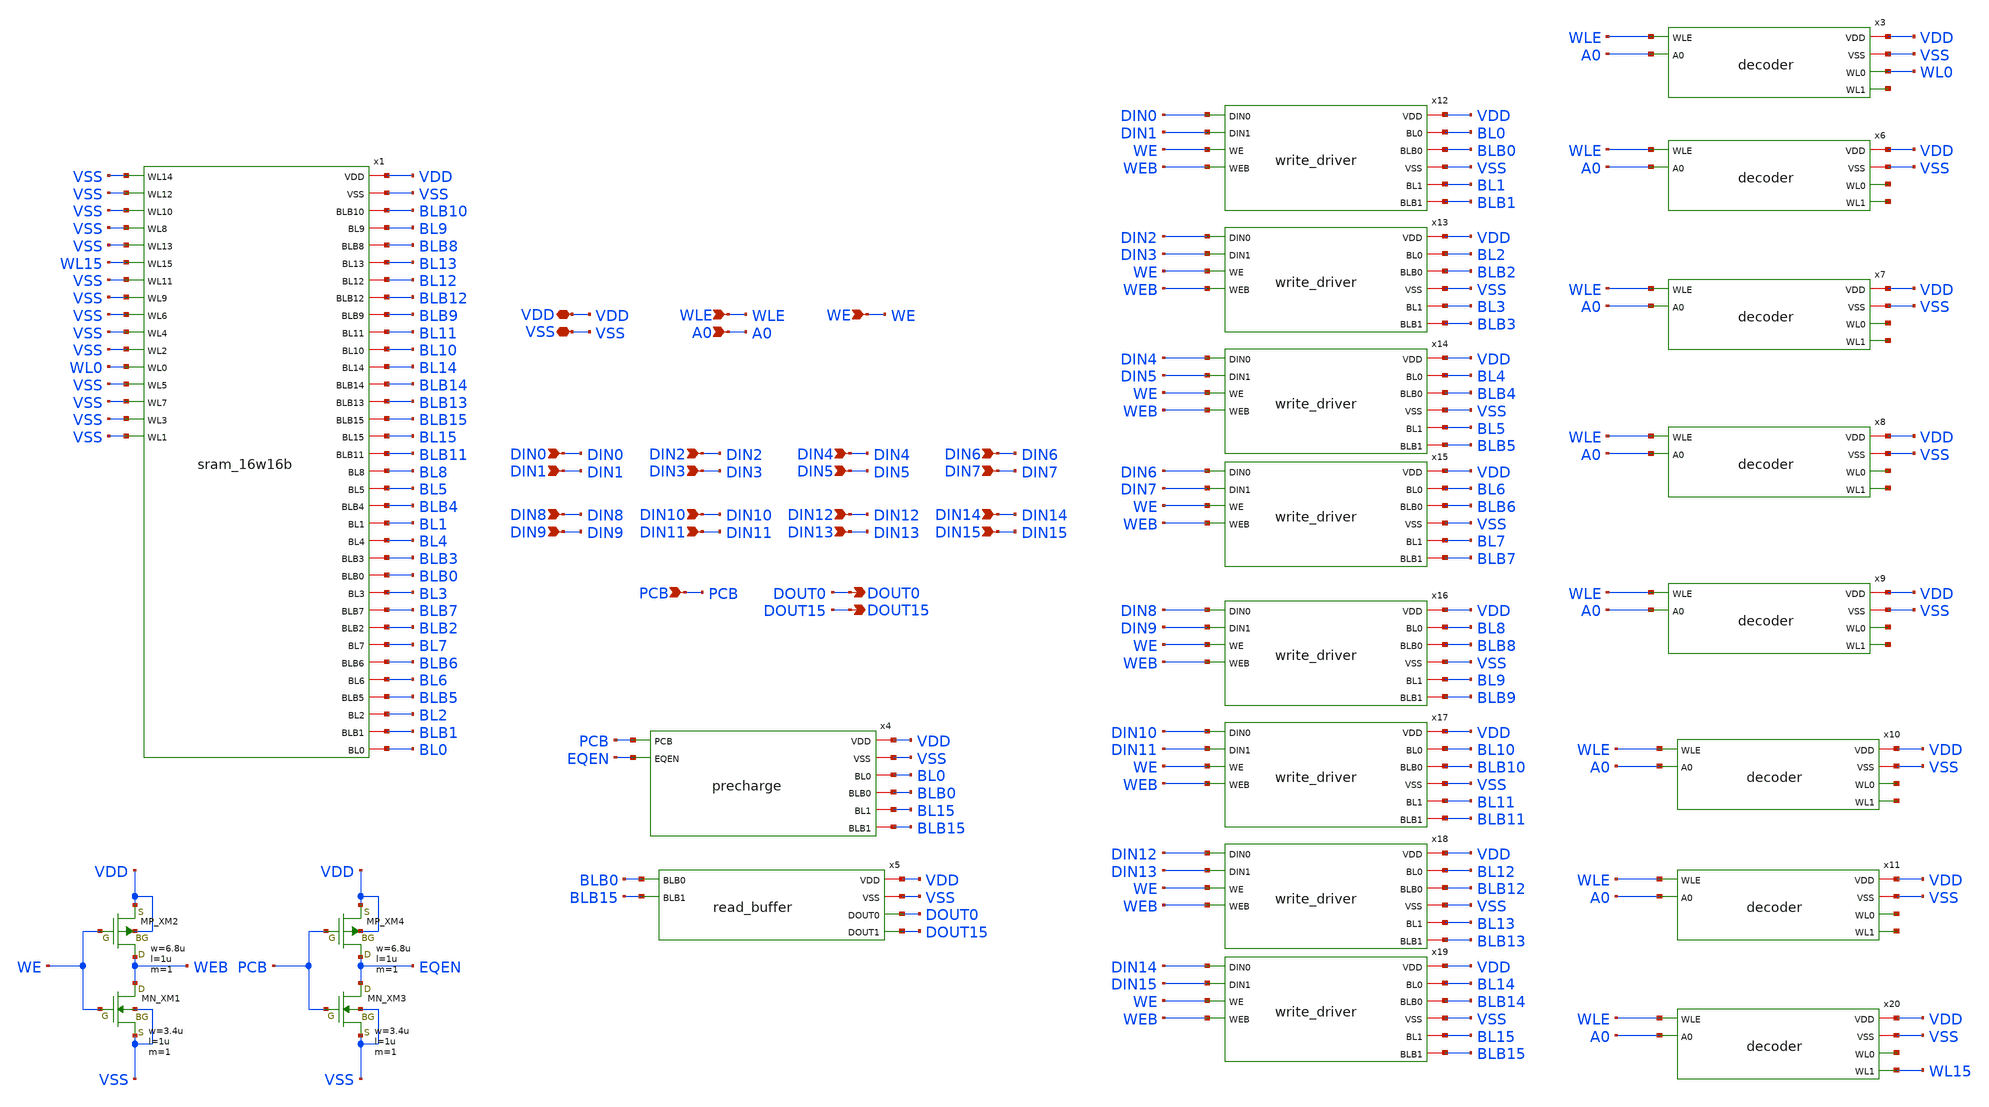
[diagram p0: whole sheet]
** sch_path: sram/sram_16w16b_top.sch
**.subckt sram_16w16b_top VDD WLE DOUT0 VSS A0 WE DIN0 DIN1 PCB DOUT15 DIN2 DIN3 DIN4 DIN5 DIN6 DIN7
*+ DIN8 DIN9 DIN10 DIN11 DIN12 DIN13 DIN14 DIN15
*.iopin VDD
*.ipin WLE
*.opin DOUT0
*.iopin VSS
*.ipin A0
*.ipin WE
*.ipin DIN0
*.ipin DIN1
*.ipin PCB
*.opin DOUT15
*.ipin DIN2
*.ipin DIN3
*.ipin DIN4
*.ipin DIN5
*.ipin DIN6
*.ipin DIN7
*.ipin DIN8
*.ipin DIN9
*.ipin DIN10
*.ipin DIN11
*.ipin DIN12
*.ipin DIN13
*.ipin DIN14
*.ipin DIN15
x4 VDD VSS PCB EQEN BL0 BLB0 BL15 BLB15 precharge
x5 VDD VSS BLB0 BLB15 DOUT0 DOUT15 read_buffer
XXM1 WEB WE VSS VSS NMOS w=3.4u l=1u nrd=0 nrs=0 m=1
XXM2 WEB WE VDD VDD PMOS w=6.8u l=1u nrd=0 nrs=0 m=1
XXM3 EQEN PCB VSS VSS NMOS w=3.4u l=1u nrd=0 nrs=0 m=1
XXM4 EQEN PCB VDD VDD PMOS w=6.8u l=1u nrd=0 nrs=0 m=1
x12 DIN0 VDD BL0 BLB0 VSS DIN1 BL1 WE BLB1 WEB write_driver
x13 DIN2 VDD BL2 BLB2 VSS DIN3 BL3 WE BLB3 WEB write_driver
x14 DIN4 VDD BL4 BLB4 VSS DIN5 BL5 WE BLB5 WEB write_driver
x15 DIN6 VDD BL6 BLB6 VSS DIN7 BL7 WE BLB7 WEB write_driver
x16 DIN8 VDD BL8 BLB8 VSS DIN9 BL9 WE BLB9 WEB write_driver
x17 DIN10 VDD BL10 BLB10 VSS DIN11 BL11 WE BLB11 WEB write_driver
x18 DIN12 VDD BL12 BLB12 VSS DIN13 BL13 WE BLB13 WEB write_driver
x19 DIN14 VDD BL14 BLB14 VSS DIN15 BL15 WE BLB15 WEB write_driver
x1 VDD VSS BLB10 BL9 BLB8 BL13 BL12 BLB12 BLB9 BL11 BL10 BL14 BLB14 BLB13 BLB15 BL15 BLB11 BL8 BL5
+ BLB4 BL1 BL4 BLB3 BLB0 BL3 BLB7 BLB2 BL7 BLB6 BL6 BLB5 BL2 BLB1 BL0 VSS VSS VSS VSS VSS WL15 VSS VSS VSS
+ VSS VSS WL0 VSS VSS VSS VSS sram_16w16b
x3 VDD VSS WL0 WLE A0 net1 decoder
x6 VDD VSS net2 WLE A0 net3 decoder
x7 VDD VSS net4 WLE A0 net5 decoder
x8 VDD VSS net6 WLE A0 net7 decoder
x9 VDD VSS net8 WLE A0 net9 decoder
x10 VDD VSS net10 WLE A0 net11 decoder
x11 VDD VSS net12 WLE A0 net13 decoder
x20 VDD VSS net14 WLE A0 WL15 decoder
**.ends
.end
